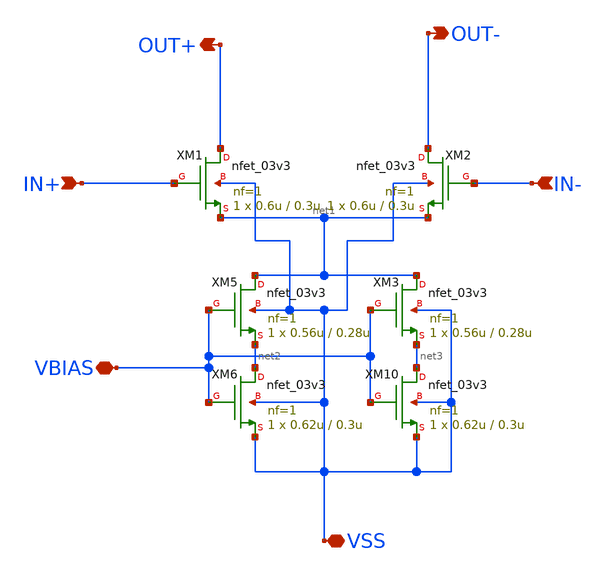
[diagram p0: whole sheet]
** sch_path: xschem/CS_Switch_16x.sch
**.subckt CS_Switch_16x IN+ IN- OUT+ OUT- VBIAS VSS
*.ipin IN+
*.ipin IN-
*.opin OUT+
*.opin OUT-
*.iopin VBIAS
*.iopin VSS
XM1 OUT+ IN+ net1 VSS nfet_03v3 L=0.3u W=0.6u nf=1 ad='int((nf+1)/2) * W/nf * 0.18u' as='int((nf+2)/2) * W/nf * 0.18u'
+ pd='2*int((nf+1)/2) * (W/nf + 0.18u)' ps='2*int((nf+2)/2) * (W/nf + 0.18u)' nrd='0.18u / W' nrs='0.18u / W'
+ sa=0 sb=0 sd=0 m=1
XM5 net1 VBIAS net2 VSS nfet_03v3 L=0.28u W=0.56u nf=1 ad='int((nf+1)/2) * W/nf * 0.18u' as='int((nf+2)/2) * W/nf * 0.18u'
+ pd='2*int((nf+1)/2) * (W/nf + 0.18u)' ps='2*int((nf+2)/2) * (W/nf + 0.18u)' nrd='0.18u / W' nrs='0.18u / W'
+ sa=0 sb=0 sd=0 m=1
XM6 net2 VBIAS VSS VSS nfet_03v3 L=0.3u W=0.62u nf=1 ad='int((nf+1)/2) * W/nf * 0.18u' as='int((nf+2)/2) * W/nf * 0.18u'
+ pd='2*int((nf+1)/2) * (W/nf + 0.18u)' ps='2*int((nf+2)/2) * (W/nf + 0.18u)' nrd='0.18u / W' nrs='0.18u / W'
+ sa=0 sb=0 sd=0 m=1
XM10 net3 VBIAS VSS VSS nfet_03v3 L=0.3u W=0.62u nf=1 ad='int((nf+1)/2) * W/nf * 0.18u' as='int((nf+2)/2) * W/nf * 0.18u'
+ pd='2*int((nf+1)/2) * (W/nf + 0.18u)' ps='2*int((nf+2)/2) * (W/nf + 0.18u)' nrd='0.18u / W' nrs='0.18u / W'
+ sa=0 sb=0 sd=0 m=1
XM3 net1 VBIAS net3 VSS nfet_03v3 L=0.28u W=0.56u nf=1 ad='int((nf+1)/2) * W/nf * 0.18u' as='int((nf+2)/2) * W/nf * 0.18u'
+ pd='2*int((nf+1)/2) * (W/nf + 0.18u)' ps='2*int((nf+2)/2) * (W/nf + 0.18u)' nrd='0.18u / W' nrs='0.18u / W'
+ sa=0 sb=0 sd=0 m=1
XM2 OUT- IN- net1 VSS nfet_03v3 L=0.3u W=0.6u nf=1 ad='int((nf+1)/2) * W/nf * 0.18u' as='int((nf+2)/2) * W/nf * 0.18u'
+ pd='2*int((nf+1)/2) * (W/nf + 0.18u)' ps='2*int((nf+2)/2) * (W/nf + 0.18u)' nrd='0.18u / W' nrs='0.18u / W'
+ sa=0 sb=0 sd=0 m=1
**.ends
.end
